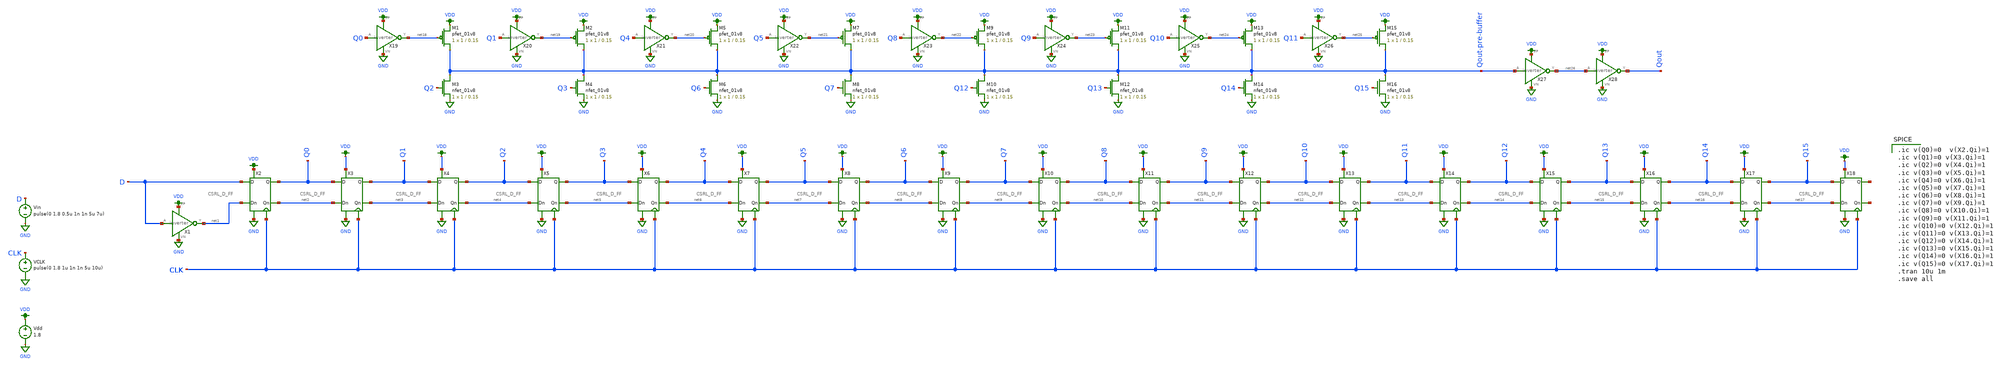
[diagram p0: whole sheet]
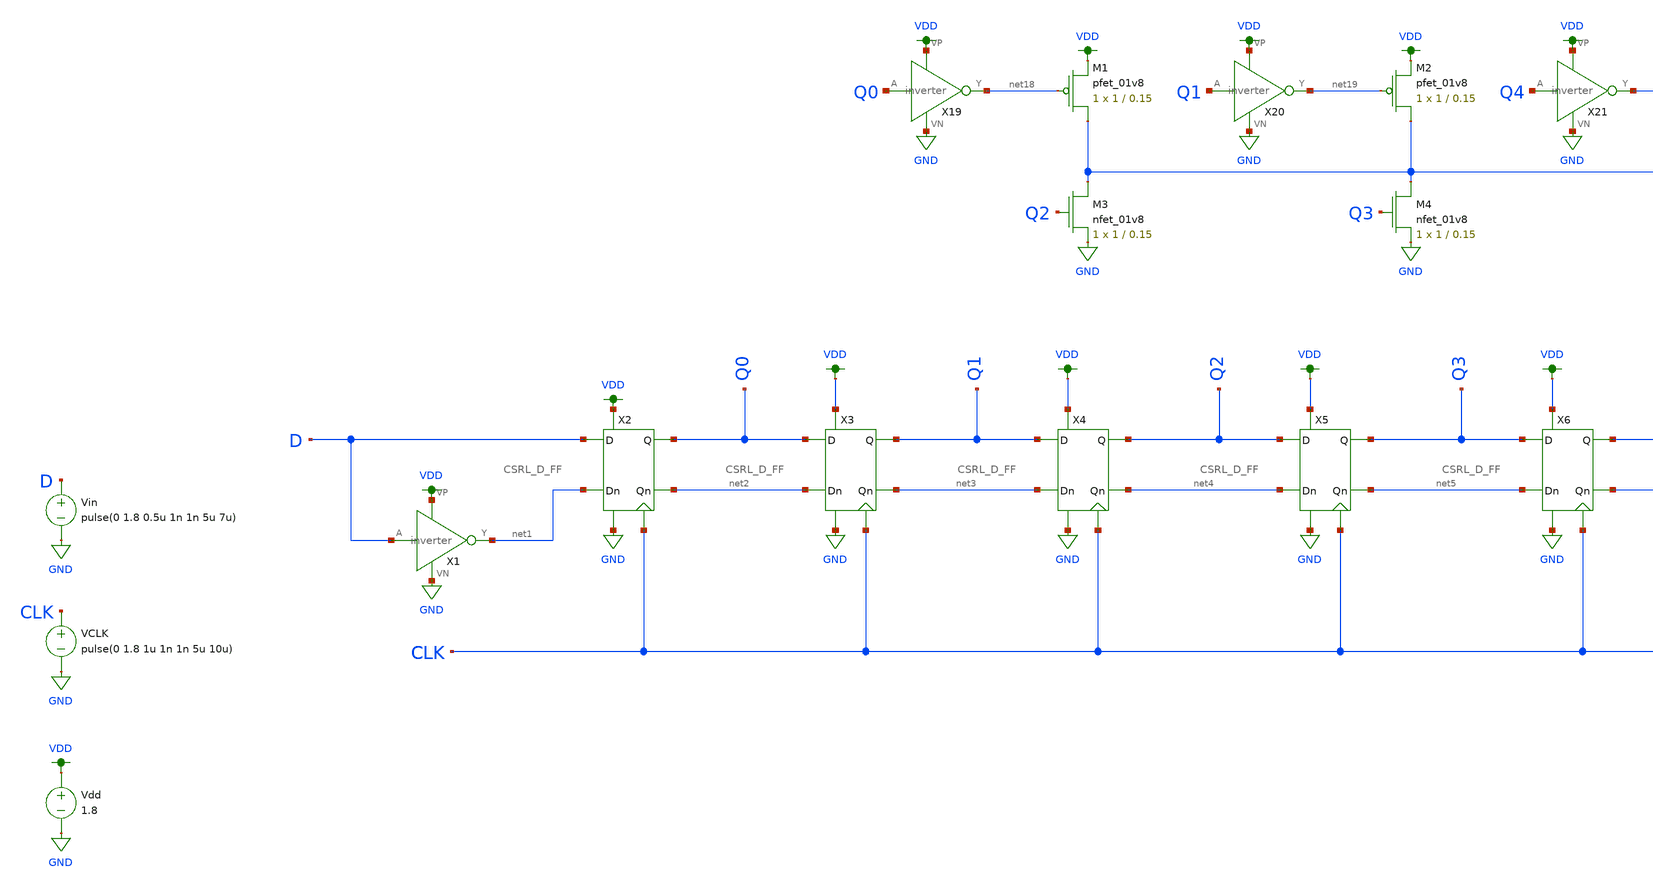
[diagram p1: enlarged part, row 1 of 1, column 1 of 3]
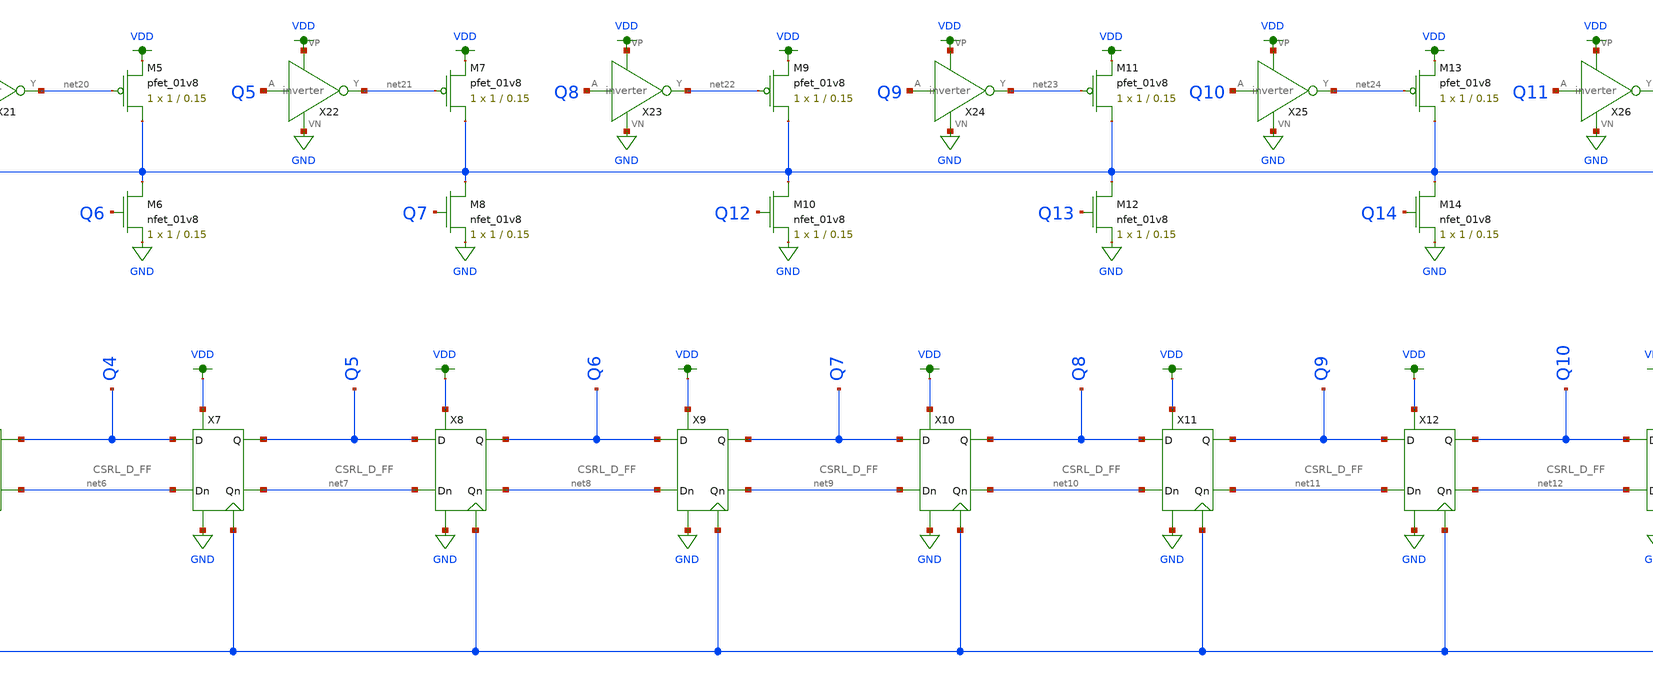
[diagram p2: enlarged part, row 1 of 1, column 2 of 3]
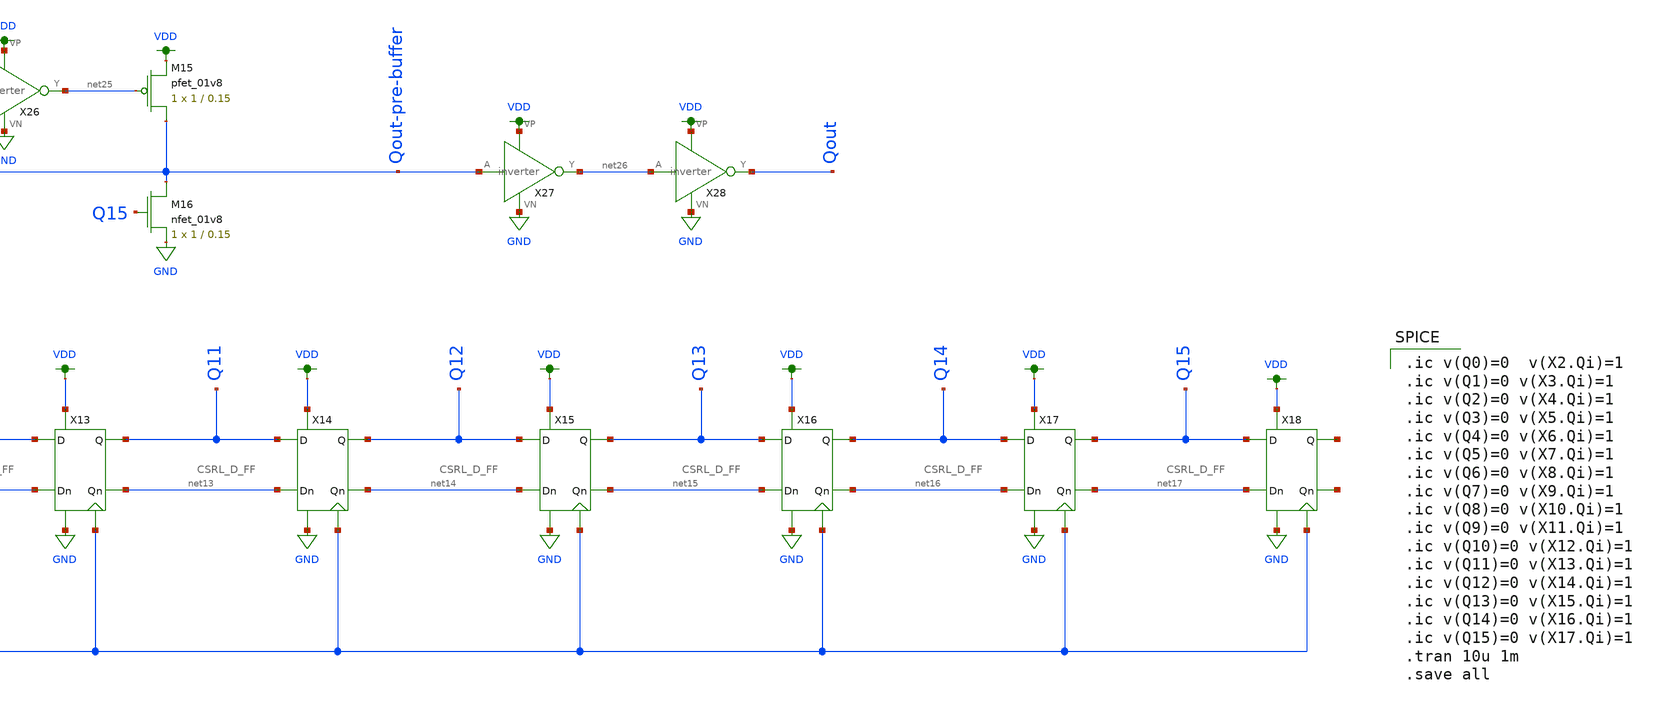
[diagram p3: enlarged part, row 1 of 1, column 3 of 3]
** sch_path: schematic/archive/phi1-new.sch
**.subckt phi1-new
Vin D GND pulse(0 1.8 0.5u 1n 1n 5u 7u)
VCLK CLK GND pulse(0 1.8 1u 1n 1n 5u 10u)
Vdd VDD GND 1.8
X1 D net1 VDD GND inverter
X2 net1 D net2 Q0 GND VDD CLK CSRL_D_FF
X3 net2 Q0 net3 Q1 GND VDD CLK CSRL_D_FF
X4 net3 Q1 net4 Q2 GND VDD CLK CSRL_D_FF
X5 net4 Q2 net5 Q3 GND VDD CLK CSRL_D_FF
X6 net5 Q3 net6 Q4 GND VDD CLK CSRL_D_FF
X7 net6 Q4 net7 Q5 GND VDD CLK CSRL_D_FF
X8 net7 Q5 net8 Q6 GND VDD CLK CSRL_D_FF
X9 net8 Q6 net9 Q7 GND VDD CLK CSRL_D_FF
X10 net9 Q7 net10 Q8 GND VDD CLK CSRL_D_FF
X11 net10 Q8 net11 Q9 GND VDD CLK CSRL_D_FF
X12 net11 Q9 net12 Q10 GND VDD CLK CSRL_D_FF
X13 net12 Q10 net13 Q11 GND VDD CLK CSRL_D_FF
X14 net13 Q11 net14 Q12 GND VDD CLK CSRL_D_FF
X15 net14 Q12 net15 Q13 GND VDD CLK CSRL_D_FF
X16 net15 Q13 net16 Q14 GND VDD CLK CSRL_D_FF
X18 net17 Q15 net27 net28 GND VDD CLK CSRL_D_FF
X17 net16 Q14 net17 Q15 GND VDD CLK CSRL_D_FF
XM1 Qout-pre-buffer net18 VDD VDD sky130_fd_pr__pfet_01v8 L=0.15 W=1 nf=1 ad='int((nf+1)/2) * W/nf * 0.29'
+ as='int((nf+2)/2) * W/nf * 0.29' pd='2*int((nf+1)/2) * (W/nf + 0.29)' ps='2*int((nf+2)/2) * (W/nf + 0.29)'
+ nrd='0.29 / W' nrs='0.29 / W' sa=0 sb=0 sd=0 mult=1 m=1
XM2 Qout-pre-buffer net19 VDD VDD sky130_fd_pr__pfet_01v8 L=0.15 W=1 nf=1 ad='int((nf+1)/2) * W/nf * 0.29'
+ as='int((nf+2)/2) * W/nf * 0.29' pd='2*int((nf+1)/2) * (W/nf + 0.29)' ps='2*int((nf+2)/2) * (W/nf + 0.29)'
+ nrd='0.29 / W' nrs='0.29 / W' sa=0 sb=0 sd=0 mult=1 m=1
X19 Q0 net18 VDD GND inverter
X20 Q1 net19 VDD GND inverter
XM3 Qout-pre-buffer Q2 GND GND sky130_fd_pr__nfet_01v8 L=0.15 W=1 nf=1 ad='int((nf+1)/2) * W/nf * 0.29'
+ as='int((nf+2)/2) * W/nf * 0.29' pd='2*int((nf+1)/2) * (W/nf + 0.29)' ps='2*int((nf+2)/2) * (W/nf + 0.29)'
+ nrd='0.29 / W' nrs='0.29 / W' sa=0 sb=0 sd=0 mult=1 m=1
XM4 Qout-pre-buffer Q3 GND GND sky130_fd_pr__nfet_01v8 L=0.15 W=1 nf=1 ad='int((nf+1)/2) * W/nf * 0.29'
+ as='int((nf+2)/2) * W/nf * 0.29' pd='2*int((nf+1)/2) * (W/nf + 0.29)' ps='2*int((nf+2)/2) * (W/nf + 0.29)'
+ nrd='0.29 / W' nrs='0.29 / W' sa=0 sb=0 sd=0 mult=1 m=1
XM5 Qout-pre-buffer net20 VDD VDD sky130_fd_pr__pfet_01v8 L=0.15 W=1 nf=1 ad='int((nf+1)/2) * W/nf * 0.29'
+ as='int((nf+2)/2) * W/nf * 0.29' pd='2*int((nf+1)/2) * (W/nf + 0.29)' ps='2*int((nf+2)/2) * (W/nf + 0.29)'
+ nrd='0.29 / W' nrs='0.29 / W' sa=0 sb=0 sd=0 mult=1 m=1
X21 Q4 net20 VDD GND inverter
XM6 Qout-pre-buffer Q6 GND GND sky130_fd_pr__nfet_01v8 L=0.15 W=1 nf=1 ad='int((nf+1)/2) * W/nf * 0.29'
+ as='int((nf+2)/2) * W/nf * 0.29' pd='2*int((nf+1)/2) * (W/nf + 0.29)' ps='2*int((nf+2)/2) * (W/nf + 0.29)'
+ nrd='0.29 / W' nrs='0.29 / W' sa=0 sb=0 sd=0 mult=1 m=1
XM7 Qout-pre-buffer net21 VDD VDD sky130_fd_pr__pfet_01v8 L=0.15 W=1 nf=1 ad='int((nf+1)/2) * W/nf * 0.29'
+ as='int((nf+2)/2) * W/nf * 0.29' pd='2*int((nf+1)/2) * (W/nf + 0.29)' ps='2*int((nf+2)/2) * (W/nf + 0.29)'
+ nrd='0.29 / W' nrs='0.29 / W' sa=0 sb=0 sd=0 mult=1 m=1
X22 Q5 net21 VDD GND inverter
XM8 Qout-pre-buffer Q7 GND GND sky130_fd_pr__nfet_01v8 L=0.15 W=1 nf=1 ad='int((nf+1)/2) * W/nf * 0.29'
+ as='int((nf+2)/2) * W/nf * 0.29' pd='2*int((nf+1)/2) * (W/nf + 0.29)' ps='2*int((nf+2)/2) * (W/nf + 0.29)'
+ nrd='0.29 / W' nrs='0.29 / W' sa=0 sb=0 sd=0 mult=1 m=1
XM9 Qout-pre-buffer net22 VDD VDD sky130_fd_pr__pfet_01v8 L=0.15 W=1 nf=1 ad='int((nf+1)/2) * W/nf * 0.29'
+ as='int((nf+2)/2) * W/nf * 0.29' pd='2*int((nf+1)/2) * (W/nf + 0.29)' ps='2*int((nf+2)/2) * (W/nf + 0.29)'
+ nrd='0.29 / W' nrs='0.29 / W' sa=0 sb=0 sd=0 mult=1 m=1
X23 Q8 net22 VDD GND inverter
XM10 Qout-pre-buffer Q12 GND GND sky130_fd_pr__nfet_01v8 L=0.15 W=1 nf=1 ad='int((nf+1)/2) * W/nf * 0.29'
+ as='int((nf+2)/2) * W/nf * 0.29' pd='2*int((nf+1)/2) * (W/nf + 0.29)' ps='2*int((nf+2)/2) * (W/nf + 0.29)'
+ nrd='0.29 / W' nrs='0.29 / W' sa=0 sb=0 sd=0 mult=1 m=1
XM11 Qout-pre-buffer net23 VDD VDD sky130_fd_pr__pfet_01v8 L=0.15 W=1 nf=1 ad='int((nf+1)/2) * W/nf * 0.29'
+ as='int((nf+2)/2) * W/nf * 0.29' pd='2*int((nf+1)/2) * (W/nf + 0.29)' ps='2*int((nf+2)/2) * (W/nf + 0.29)'
+ nrd='0.29 / W' nrs='0.29 / W' sa=0 sb=0 sd=0 mult=1 m=1
X24 Q9 net23 VDD GND inverter
XM12 Qout-pre-buffer Q13 GND GND sky130_fd_pr__nfet_01v8 L=0.15 W=1 nf=1 ad='int((nf+1)/2) * W/nf * 0.29'
+ as='int((nf+2)/2) * W/nf * 0.29' pd='2*int((nf+1)/2) * (W/nf + 0.29)' ps='2*int((nf+2)/2) * (W/nf + 0.29)'
+ nrd='0.29 / W' nrs='0.29 / W' sa=0 sb=0 sd=0 mult=1 m=1
XM13 Qout-pre-buffer net24 VDD VDD sky130_fd_pr__pfet_01v8 L=0.15 W=1 nf=1 ad='int((nf+1)/2) * W/nf * 0.29'
+ as='int((nf+2)/2) * W/nf * 0.29' pd='2*int((nf+1)/2) * (W/nf + 0.29)' ps='2*int((nf+2)/2) * (W/nf + 0.29)'
+ nrd='0.29 / W' nrs='0.29 / W' sa=0 sb=0 sd=0 mult=1 m=1
X25 Q10 net24 VDD GND inverter
XM14 Qout-pre-buffer Q14 GND GND sky130_fd_pr__nfet_01v8 L=0.15 W=1 nf=1 ad='int((nf+1)/2) * W/nf * 0.29'
+ as='int((nf+2)/2) * W/nf * 0.29' pd='2*int((nf+1)/2) * (W/nf + 0.29)' ps='2*int((nf+2)/2) * (W/nf + 0.29)'
+ nrd='0.29 / W' nrs='0.29 / W' sa=0 sb=0 sd=0 mult=1 m=1
XM15 Qout-pre-buffer net25 VDD VDD sky130_fd_pr__pfet_01v8 L=0.15 W=1 nf=1 ad='int((nf+1)/2) * W/nf * 0.29'
+ as='int((nf+2)/2) * W/nf * 0.29' pd='2*int((nf+1)/2) * (W/nf + 0.29)' ps='2*int((nf+2)/2) * (W/nf + 0.29)'
+ nrd='0.29 / W' nrs='0.29 / W' sa=0 sb=0 sd=0 mult=1 m=1
X26 Q11 net25 VDD GND inverter
XM16 Qout-pre-buffer Q15 GND GND sky130_fd_pr__nfet_01v8 L=0.15 W=1 nf=1 ad='int((nf+1)/2) * W/nf * 0.29'
+ as='int((nf+2)/2) * W/nf * 0.29' pd='2*int((nf+1)/2) * (W/nf + 0.29)' ps='2*int((nf+2)/2) * (W/nf + 0.29)'
+ nrd='0.29 / W' nrs='0.29 / W' sa=0 sb=0 sd=0 mult=1 m=1
X27 Qout-pre-buffer net26 VDD GND inverter
X28 net26 Qout VDD GND inverter
**** begin user architecture code

.ic v(Q0)=0  v(X2.Qi)=1
.ic v(Q1)=0 v(X3.Qi)=1
.ic v(Q2)=0 v(X4.Qi)=1
.ic v(Q3)=0 v(X5.Qi)=1
.ic v(Q4)=0 v(X6.Qi)=1
.ic v(Q5)=0 v(X7.Qi)=1
.ic v(Q6)=0 v(X8.Qi)=1
.ic v(Q7)=0 v(X9.Qi)=1
.ic v(Q8)=0 v(X10.Qi)=1
.ic v(Q9)=0 v(X11.Qi)=1
.ic v(Q10)=0 v(X12.Qi)=1
.ic v(Q11)=0 v(X13.Qi)=1
.ic v(Q12)=0 v(X14.Qi)=1
.ic v(Q13)=0 v(X15.Qi)=1
.ic v(Q14)=0 v(X16.Qi)=1
.ic v(Q15)=0 v(X17.Qi)=1
.tran 10u 1m
.save all


.option wnflag=1
.param MC_SWITCH=0.0
.lib ~/skywater/skywater-pdk/libraries/sky130_fd_pr_ngspice/latest/models/sky130.lib.spice tt

**** end user architecture code
**.ends

* expanding   symbol:  /home/madvlsi/Documents/MADVLSI-Final_Project/schematic/inverter.sym # of
*+ pins=4
** sym_path: schematic/inverter.sym
** sch_path: schematic/inverter.sch
.subckt inverter A Y VP VN
*.opin Y
*.ipin A
*.iopin VP
*.iopin VN
XM3 Y A VP VDD sky130_fd_pr__pfet_01v8 L={Lp} W={Wp} nf=1 ad='int((nf+1)/2) * W/nf * 0.29' as='int((nf+2)/2) * W/nf * 0.29'
+ pd='2*int((nf+1)/2) * (W/nf + 0.29)' ps='2*int((nf+2)/2) * (W/nf + 0.29)' nrd='0.29 / W' nrs='0.29 / W'
+ sa=0 sb=0 sd=0 mult=1 m=1
XM4 Y A VP VDD sky130_fd_pr__pfet_01v8 L={Lp} W={Wp} nf=1 ad='int((nf+1)/2) * W/nf * 0.29' as='int((nf+2)/2) * W/nf * 0.29'
+ pd='2*int((nf+1)/2) * (W/nf + 0.29)' ps='2*int((nf+2)/2) * (W/nf + 0.29)' nrd='0.29 / W' nrs='0.29 / W'
+ sa=0 sb=0 sd=0 mult=1 m=1
XM5 Y A VN GND sky130_fd_pr__nfet_01v8 L={Lp} W={Wp} nf=1 ad='int((nf+1)/2) * W/nf * 0.29' as='int((nf+2)/2) * W/nf * 0.29'
+ pd='2*int((nf+1)/2) * (W/nf + 0.29)' ps='2*int((nf+2)/2) * (W/nf + 0.29)' nrd='0.29 / W' nrs='0.29 / W'
+ sa=0 sb=0 sd=0 mult=1 m=1
.ends


* expanding   symbol:  /home/madvlsi/Documents/MADVLSI-Final_Project/schematic/CSRL_D_FF.sym # of
*+ pins=7
** sym_path: schematic/CSRL_D_FF.sym
** sch_path: schematic/CSRL_D_FF.sch
.subckt CSRL_D_FF Dn D Qn Q VN VP CLK
*.ipin Dn
*.ipin D
*.iopin VP
*.iopin VN
*.iopin CLK
*.opin Qn
*.opin Q
XM1 net5 CLK VP VDD sky130_fd_pr__pfet_01v8 L=0.15 W=1 nf=1 ad='int((nf+1)/2) * W/nf * 0.29' as='int((nf+2)/2) * W/nf * 0.29'
+ pd='2*int((nf+1)/2) * (W/nf + 0.29)' ps='2*int((nf+2)/2) * (W/nf + 0.29)' nrd='0.29 / W' nrs='0.29 / W'
+ sa=0 sb=0 sd=0 mult=1 m=1
XM2 net6 CLK VP VDD sky130_fd_pr__pfet_01v8 L=0.15 W=1 nf=1 ad='int((nf+1)/2) * W/nf * 0.29' as='int((nf+2)/2) * W/nf * 0.29'
+ pd='2*int((nf+1)/2) * (W/nf + 0.29)' ps='2*int((nf+2)/2) * (W/nf + 0.29)' nrd='0.29 / W' nrs='0.29 / W'
+ sa=0 sb=0 sd=0 mult=1 m=1
XM3 net3 CLK Q GND sky130_fd_pr__nfet_01v8 L=0.15 W=1 nf=1 ad='int((nf+1)/2) * W/nf * 0.29' as='int((nf+2)/2) * W/nf * 0.29'
+ pd='2*int((nf+1)/2) * (W/nf + 0.29)' ps='2*int((nf+2)/2) * (W/nf + 0.29)' nrd='0.29 / W' nrs='0.29 / W'
+ sa=0 sb=0 sd=0 mult=1 m=1
XM4 net4 CLK Qn GND sky130_fd_pr__nfet_01v8 L=0.15 W=1 nf=1 ad='int((nf+1)/2) * W/nf * 0.29' as='int((nf+2)/2) * W/nf * 0.29'
+ pd='2*int((nf+1)/2) * (W/nf + 0.29)' ps='2*int((nf+2)/2) * (W/nf + 0.29)' nrd='0.29 / W' nrs='0.29 / W'
+ sa=0 sb=0 sd=0 mult=1 m=1
XM5 Q Qn net6 VDD sky130_fd_pr__pfet_01v8 L=0.15 W=1 nf=1 ad='int((nf+1)/2) * W/nf * 0.29' as='int((nf+2)/2) * W/nf * 0.29'
+ pd='2*int((nf+1)/2) * (W/nf + 0.29)' ps='2*int((nf+2)/2) * (W/nf + 0.29)' nrd='0.29 / W' nrs='0.29 / W'
+ sa=0 sb=0 sd=0 mult=1 m=1
XM6 VN Qn Q GND sky130_fd_pr__nfet_01v8 L=0.15 W=1 nf=1 ad='int((nf+1)/2) * W/nf * 0.29' as='int((nf+2)/2) * W/nf * 0.29'
+ pd='2*int((nf+1)/2) * (W/nf + 0.29)' ps='2*int((nf+2)/2) * (W/nf + 0.29)' nrd='0.29 / W' nrs='0.29 / W'
+ sa=0 sb=0 sd=0 mult=1 m=1
XM7 Qn Q net5 VDD sky130_fd_pr__pfet_01v8 L=0.15 W=1 nf=1 ad='int((nf+1)/2) * W/nf * 0.29' as='int((nf+2)/2) * W/nf * 0.29'
+ pd='2*int((nf+1)/2) * (W/nf + 0.29)' ps='2*int((nf+2)/2) * (W/nf + 0.29)' nrd='0.29 / W' nrs='0.29 / W'
+ sa=0 sb=0 sd=0 mult=1 m=1
XM8 VN Q Qn GND sky130_fd_pr__nfet_01v8 L=0.15 W=1 nf=1 ad='int((nf+1)/2) * W/nf * 0.29' as='int((nf+2)/2) * W/nf * 0.29'
+ pd='2*int((nf+1)/2) * (W/nf + 0.29)' ps='2*int((nf+2)/2) * (W/nf + 0.29)' nrd='0.29 / W' nrs='0.29 / W'
+ sa=0 sb=0 sd=0 mult=1 m=1
XM9 net4 CLK Dn VDD sky130_fd_pr__pfet_01v8 L=0.15 W=1 nf=1 ad='int((nf+1)/2) * W/nf * 0.29' as='int((nf+2)/2) * W/nf * 0.29'
+ pd='2*int((nf+1)/2) * (W/nf + 0.29)' ps='2*int((nf+2)/2) * (W/nf + 0.29)' nrd='0.29 / W' nrs='0.29 / W'
+ sa=0 sb=0 sd=0 mult=1 m=1
XM10 net3 CLK D VDD sky130_fd_pr__pfet_01v8 L=0.15 W=1 nf=1 ad='int((nf+1)/2) * W/nf * 0.29' as='int((nf+2)/2) * W/nf * 0.29'
+ pd='2*int((nf+1)/2) * (W/nf + 0.29)' ps='2*int((nf+2)/2) * (W/nf + 0.29)' nrd='0.29 / W' nrs='0.29 / W'
+ sa=0 sb=0 sd=0 mult=1 m=1
XM11 VN CLK net1 GND sky130_fd_pr__nfet_01v8 L=0.15 W=1 nf=1 ad='int((nf+1)/2) * W/nf * 0.29' as='int((nf+2)/2) * W/nf * 0.29'
+ pd='2*int((nf+1)/2) * (W/nf + 0.29)' ps='2*int((nf+2)/2) * (W/nf + 0.29)' nrd='0.29 / W' nrs='0.29 / W'
+ sa=0 sb=0 sd=0 mult=1 m=1
XM12 VN CLK net2 GND sky130_fd_pr__nfet_01v8 L=0.15 W=1 nf=1 ad='int((nf+1)/2) * W/nf * 0.29' as='int((nf+2)/2) * W/nf * 0.29'
+ pd='2*int((nf+1)/2) * (W/nf + 0.29)' ps='2*int((nf+2)/2) * (W/nf + 0.29)' nrd='0.29 / W' nrs='0.29 / W'
+ sa=0 sb=0 sd=0 mult=1 m=1
XM13 VP net3 net4 VDD sky130_fd_pr__pfet_01v8 L=0.15 W=1 nf=1 ad='int((nf+1)/2) * W/nf * 0.29' as='int((nf+2)/2) * W/nf * 0.29'
+ pd='2*int((nf+1)/2) * (W/nf + 0.29)' ps='2*int((nf+2)/2) * (W/nf + 0.29)' nrd='0.29 / W' nrs='0.29 / W'
+ sa=0 sb=0 sd=0 mult=1 m=1
XM14 VP net4 net3 VDD sky130_fd_pr__pfet_01v8 L=0.15 W=1 nf=1 ad='int((nf+1)/2) * W/nf * 0.29' as='int((nf+2)/2) * W/nf * 0.29'
+ pd='2*int((nf+1)/2) * (W/nf + 0.29)' ps='2*int((nf+2)/2) * (W/nf + 0.29)' nrd='0.29 / W' nrs='0.29 / W'
+ sa=0 sb=0 sd=0 mult=1 m=1
XM15 net3 net4 net1 GND sky130_fd_pr__nfet_01v8 L=0.15 W=1 nf=1 ad='int((nf+1)/2) * W/nf * 0.29' as='int((nf+2)/2) * W/nf * 0.29'
+ pd='2*int((nf+1)/2) * (W/nf + 0.29)' ps='2*int((nf+2)/2) * (W/nf + 0.29)' nrd='0.29 / W' nrs='0.29 / W'
+ sa=0 sb=0 sd=0 mult=1 m=1
XM16 net4 net3 net2 GND sky130_fd_pr__nfet_01v8 L=0.15 W=1 nf=1 ad='int((nf+1)/2) * W/nf * 0.29' as='int((nf+2)/2) * W/nf * 0.29'
+ pd='2*int((nf+1)/2) * (W/nf + 0.29)' ps='2*int((nf+2)/2) * (W/nf + 0.29)' nrd='0.29 / W' nrs='0.29 / W'
+ sa=0 sb=0 sd=0 mult=1 m=1
XM17 VN CLK net2 GND sky130_fd_pr__nfet_01v8 L=0.15 W=1 nf=1 ad='int((nf+1)/2) * W/nf * 0.29' as='int((nf+2)/2) * W/nf * 0.29'
+ pd='2*int((nf+1)/2) * (W/nf + 0.29)' ps='2*int((nf+2)/2) * (W/nf + 0.29)' nrd='0.29 / W' nrs='0.29 / W'
+ sa=0 sb=0 sd=0 mult=1 m=1
XM18 VN CLK net1 GND sky130_fd_pr__nfet_01v8 L=0.15 W=1 nf=1 ad='int((nf+1)/2) * W/nf * 0.29' as='int((nf+2)/2) * W/nf * 0.29'
+ pd='2*int((nf+1)/2) * (W/nf + 0.29)' ps='2*int((nf+2)/2) * (W/nf + 0.29)' nrd='0.29 / W' nrs='0.29 / W'
+ sa=0 sb=0 sd=0 mult=1 m=1
.ends

.GLOBAL GND
.GLOBAL VDD
.end
